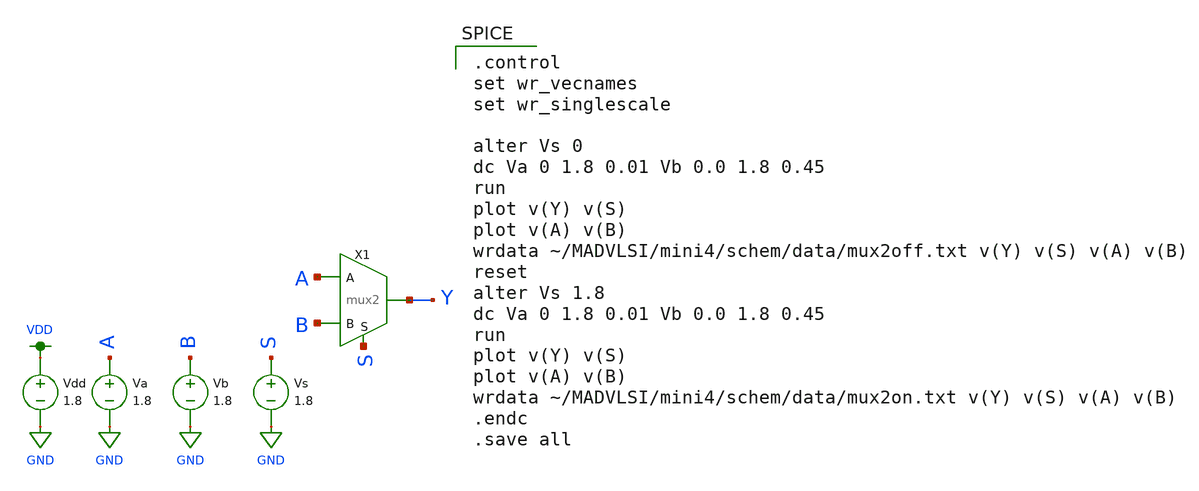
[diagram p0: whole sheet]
** sch_path: mini4/schem/mux2test.sch
**.subckt mux2test
X1 Y A B S mux2
Va A GND 1.8
Vb B GND 1.8
Vdd VDD GND 1.8
Vs S GND 1.8
**** begin user architecture code

.option wnflag=1
.param MC_SWITCH=1.0
.lib ~/skywater/skywater-pdk/libraries/sky130_fd_pr_ngspice/latest/models/sky130.lib.spice tt


.control
set wr_vecnames
set wr_singlescale

alter Vs 0
dc Va 0 1.8 0.01 Vb 0.0 1.8 0.45
run
plot v(Y) v(S)
plot v(A) v(B)
wrdata ~/MADVLSI/mini4/schem/data/mux2off.txt v(Y) v(S) v(A) v(B)
reset
alter Vs 1.8
dc Va 0 1.8 0.01 Vb 0.0 1.8 0.45
run
plot v(Y) v(S)
plot v(A) v(B)
wrdata ~/MADVLSI/mini4/schem/data/mux2on.txt v(Y) v(S) v(A) v(B)
.endc
.save all


**** end user architecture code
**.ends
.GLOBAL GND
.GLOBAL VDD
.end
